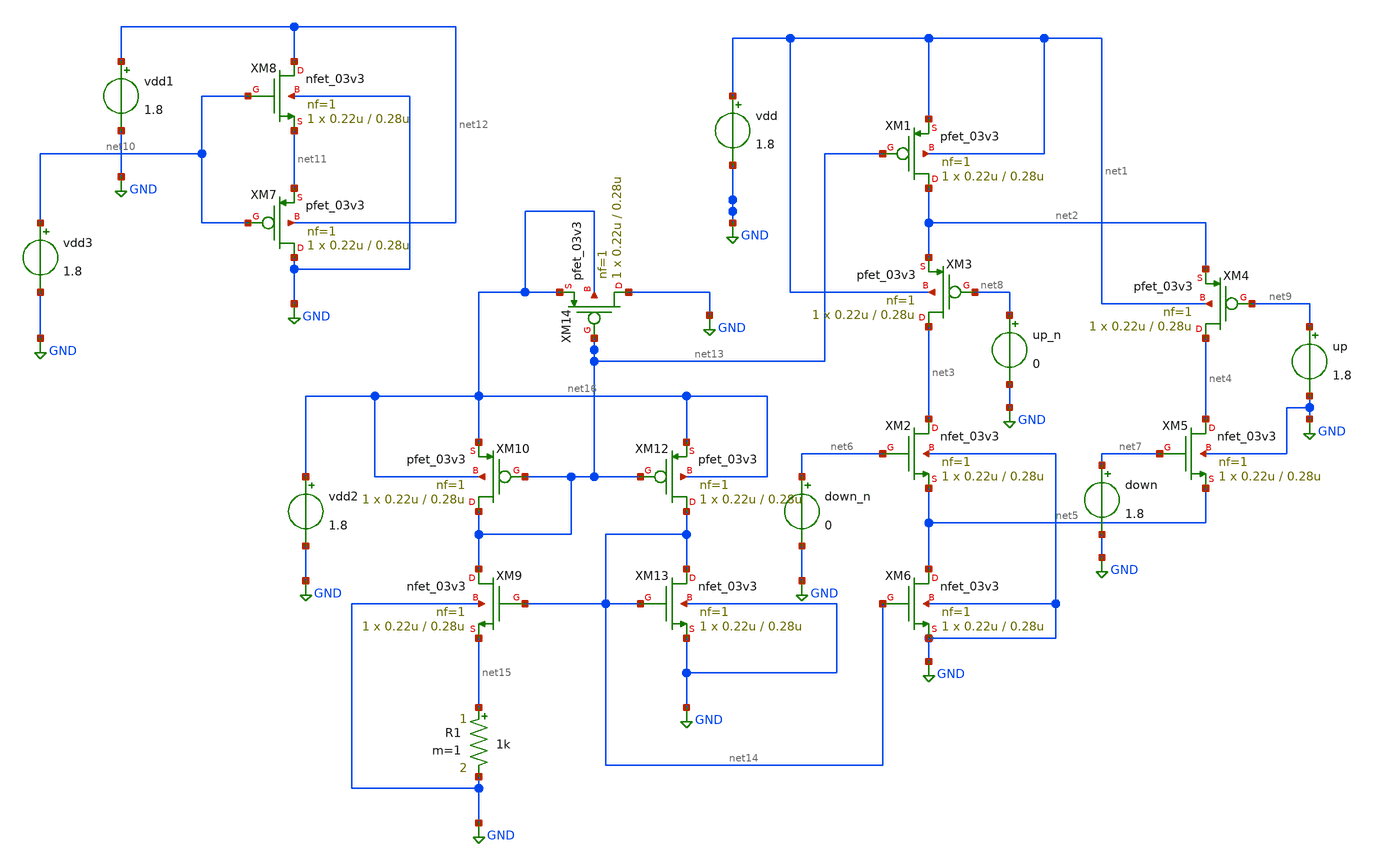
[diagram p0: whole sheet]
** sch_path: src/ChargePump/cp_amp.sch
* Copyright 2022 GlobalFoundries PDK Authors
* Licensed under the Apache License, Version 2.0 (the "License");
* you may not use this file except in compliance with the License.
* You may obtain a copy of the License at
* https://www.apache.org/licenses/LICENSE-2.0
* Unless required by applicable law or agreed to in writing, software
* distributed under the License is distributed on an "AS IS" BASIS,
* WITHOUT WARRANTIES OR CONDITIONS OF ANY KIND, either express or implied.
* See the License for the specific language governing permissions and
* limitations under the License.
**.subckt cp_amp
XM1 net2 net13 net1 net1 pfet_03v3 L=0.28u W=0.22u nf=1 ad='int((nf+1)/2) * W/nf * 0.18u' as='int((nf+2)/2) * W/nf * 0.18u'
+ pd='2*int((nf+1)/2) * (W/nf + 0.18u)' ps='2*int((nf+2)/2) * (W/nf + 0.18u)' nrd='0.18u / W' nrs='0.18u / W'
+ sa=0 sb=0 sd=0 m=1
XM2 net3 net6 net5 GND nfet_03v3 L=0.28u W=0.22u nf=1 ad='int((nf+1)/2) * W/nf * 0.18u' as='int((nf+2)/2) * W/nf * 0.18u'
+ pd='2*int((nf+1)/2) * (W/nf + 0.18u)' ps='2*int((nf+2)/2) * (W/nf + 0.18u)' nrd='0.18u / W' nrs='0.18u / W'
+ sa=0 sb=0 sd=0 m=1
vdd net1 GND 1.8
XM3 net3 net8 net2 net1 pfet_03v3 L=0.28u W=0.22u nf=1 ad='int((nf+1)/2) * W/nf * 0.18u' as='int((nf+2)/2) * W/nf * 0.18u'
+ pd='2*int((nf+1)/2) * (W/nf + 0.18u)' ps='2*int((nf+2)/2) * (W/nf + 0.18u)' nrd='0.18u / W' nrs='0.18u / W'
+ sa=0 sb=0 sd=0 m=1
XM4 net4 net9 net2 net1 pfet_03v3 L=0.28u W=0.22u nf=1 ad='int((nf+1)/2) * W/nf * 0.18u' as='int((nf+2)/2) * W/nf * 0.18u'
+ pd='2*int((nf+1)/2) * (W/nf + 0.18u)' ps='2*int((nf+2)/2) * (W/nf + 0.18u)' nrd='0.18u / W' nrs='0.18u / W'
+ sa=0 sb=0 sd=0 m=1
XM5 net4 net7 net5 GND nfet_03v3 L=0.28u W=0.22u nf=1 ad='int((nf+1)/2) * W/nf * 0.18u' as='int((nf+2)/2) * W/nf * 0.18u'
+ pd='2*int((nf+1)/2) * (W/nf + 0.18u)' ps='2*int((nf+2)/2) * (W/nf + 0.18u)' nrd='0.18u / W' nrs='0.18u / W'
+ sa=0 sb=0 sd=0 m=1
XM6 net5 net14 GND GND nfet_03v3 L=0.28u W=0.22u nf=1 ad='int((nf+1)/2) * W/nf * 0.18u' as='int((nf+2)/2) * W/nf * 0.18u'
+ pd='2*int((nf+1)/2) * (W/nf + 0.18u)' ps='2*int((nf+2)/2) * (W/nf + 0.18u)' nrd='0.18u / W' nrs='0.18u / W'
+ sa=0 sb=0 sd=0 m=1
down net7 GND 1.8
up net9 GND 1.8
up_n net8 GND 0
down_n net6 GND 0
XM7 GND net10 net11 net12 pfet_03v3 L=0.28u W=0.22u nf=1 ad='int((nf+1)/2) * W/nf * 0.18u' as='int((nf+2)/2) * W/nf * 0.18u'
+ pd='2*int((nf+1)/2) * (W/nf + 0.18u)' ps='2*int((nf+2)/2) * (W/nf + 0.18u)' nrd='0.18u / W' nrs='0.18u / W'
+ sa=0 sb=0 sd=0 m=1
XM8 net12 net10 net11 GND nfet_03v3 L=0.28u W=0.22u nf=1 ad='int((nf+1)/2) * W/nf * 0.18u' as='int((nf+2)/2) * W/nf * 0.18u'
+ pd='2*int((nf+1)/2) * (W/nf + 0.18u)' ps='2*int((nf+2)/2) * (W/nf + 0.18u)' nrd='0.18u / W' nrs='0.18u / W'
+ sa=0 sb=0 sd=0 m=1
vdd1 net12 GND 1.8
vdd2 net16 GND 1.8
XM10 net13 net13 net16 net16 pfet_03v3 L=0.28u W=0.22u nf=1 ad='int((nf+1)/2) * W/nf * 0.18u' as='int((nf+2)/2) * W/nf * 0.18u'
+ pd='2*int((nf+1)/2) * (W/nf + 0.18u)' ps='2*int((nf+2)/2) * (W/nf + 0.18u)' nrd='0.18u / W' nrs='0.18u / W'
+ sa=0 sb=0 sd=0 m=1
XM9 net13 net14 net15 GND nfet_03v3 L=0.28u W=0.22u nf=1 ad='int((nf+1)/2) * W/nf * 0.18u' as='int((nf+2)/2) * W/nf * 0.18u'
+ pd='2*int((nf+1)/2) * (W/nf + 0.18u)' ps='2*int((nf+2)/2) * (W/nf + 0.18u)' nrd='0.18u / W' nrs='0.18u / W'
+ sa=0 sb=0 sd=0 m=1
R1 net15 GND 1k m=1
XM12 net14 net13 net16 net16 pfet_03v3 L=0.28u W=0.22u nf=1 ad='int((nf+1)/2) * W/nf * 0.18u' as='int((nf+2)/2) * W/nf * 0.18u'
+ pd='2*int((nf+1)/2) * (W/nf + 0.18u)' ps='2*int((nf+2)/2) * (W/nf + 0.18u)' nrd='0.18u / W' nrs='0.18u / W'
+ sa=0 sb=0 sd=0 m=1
XM13 net14 net14 GND GND nfet_03v3 L=0.28u W=0.22u nf=1 ad='int((nf+1)/2) * W/nf * 0.18u' as='int((nf+2)/2) * W/nf * 0.18u'
+ pd='2*int((nf+1)/2) * (W/nf + 0.18u)' ps='2*int((nf+2)/2) * (W/nf + 0.18u)' nrd='0.18u / W' nrs='0.18u / W'
+ sa=0 sb=0 sd=0 m=1
XM14 GND net13 net16 net16 pfet_03v3 L=0.28u W=0.22u nf=1 ad='int((nf+1)/2) * W/nf * 0.18u' as='int((nf+2)/2) * W/nf * 0.18u'
+ pd='2*int((nf+1)/2) * (W/nf + 0.18u)' ps='2*int((nf+2)/2) * (W/nf + 0.18u)' nrd='0.18u / W' nrs='0.18u / W'
+ sa=0 sb=0 sd=0 m=1
vdd3 net10 GND 1.8
**.ends
.GLOBAL GND
.end
